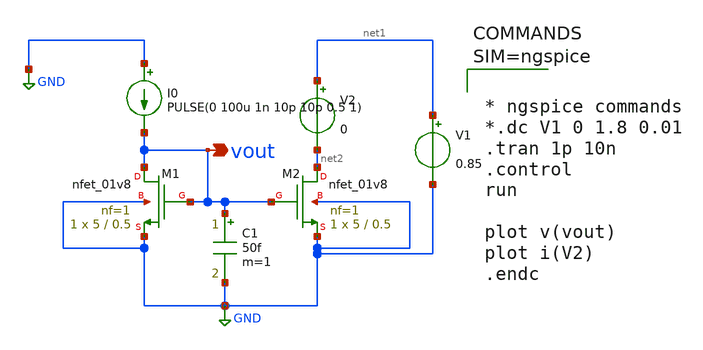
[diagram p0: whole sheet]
** sch_path: xschem/curr_mirr_cap.sch
**.subckt curr_mirr_cap vout
*.opin vout
XM2 net2 vout GND GND sky130_fd_pr__nfet_01v8 L=0.5 W=5 nf=1 ad='int((1 + 1)/2) * 5 / 1 * 0.29' as='int((1 + 2)/2) * 5 / 1 * 0.29'
+ pd='2*int((1 + 1)/2) * (5 / 1 + 0.29)' ps='2*int((1 + 2)/2) * (5 / 1 + 0.29)' nrd='0.29 / 5 ' nrs='0.29 / 5 '
+ sa=0 sb=0 sd=0 mult=1 m=1
XM1 vout vout GND GND sky130_fd_pr__nfet_01v8 L=0.5 W=5 nf=1 ad='int((1 + 1)/2) * 5 / 1 * 0.29' as='int((1 + 2)/2) * 5 / 1 * 0.29'
+ pd='2*int((1 + 1)/2) * (5 / 1 + 0.29)' ps='2*int((1 + 2)/2) * (5 / 1 + 0.29)' nrd='0.29 / 5 ' nrs='0.29 / 5 '
+ sa=0 sb=0 sd=0 mult=1 m=1
I0 GND vout PULSE(0 100u 1n 10p 10p 0.5 1)
V1 net1 GND 0.85
V2 net1 net2 0
C1 vout GND 50f m=1
**** begin user architecture code

** opencircuitdesign pdks install
.lib $::SKYWATER_MODELS/sky130.lib.spice tt




* ngspice commands
*.dc V1 0 1.8 0.01
.tran 1p 10n
.control
run

plot v(vout)
plot i(V2)
.endc



**** end user architecture code
**.ends
.GLOBAL GND
.end
